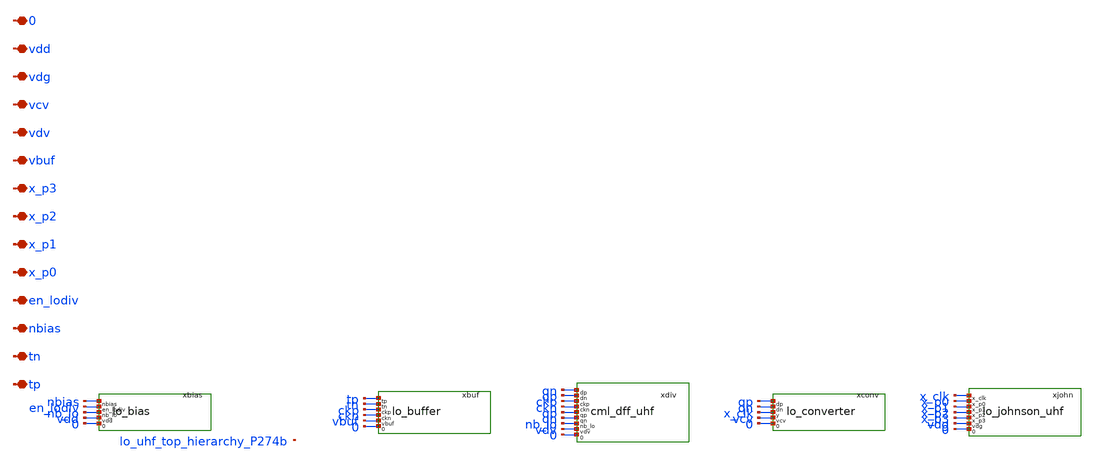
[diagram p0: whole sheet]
** sch_path: analog/lo/sch/lo_uhf_top.sch
**.subckt lo_uhf_top tp tn nbias en_lodiv x_p0 x_p1 x_p2 x_p3 vbuf vdv vcv vdg vdd 0
*.iopin tp
*.iopin tn
*.iopin nbias
*.iopin en_lodiv
*.iopin x_p0
*.iopin x_p1
*.iopin x_p2
*.iopin x_p3
*.iopin vbuf
*.iopin vdv
*.iopin vcv
*.iopin vdg
*.iopin vdd
*.iopin 0
xbias nbias en_lodiv nb_lo vdd 0 lo_bias
xbuf tp tn ckp ckn vbuf 0 lo_buffer
xdiv qn qp ckp ckn qp qn nb_lo vdv 0 cml_dff_uhf
xconv qp qn x_clk vcv 0 lo_converter
xjohn x_clk x_p0 x_p1 x_p2 x_p3 vdg 0 lo_johnson_uhf
**.ends

* expanding   symbol:  lo_bias.sym # of pins=5
** sym_path: analog/lo/sch/lo_bias.sym
** sch_path: analog/lo/sch/lo_bias.sch
.subckt lo_bias nbias en_lodiv nb_lo vdd 0
*.iopin nbias
*.iopin en_lodiv
*.iopin nb_lo
*.iopin vdd
*.iopin 0
Xxenb_p en_n en_lodiv vdd vdd sg13_lv_pmos w=1u l=0.13u ng=1 m=1 mm_ok=1
Xxenb_n en_n en_lodiv 0 0 sg13_lv_nmos w=0.5u l=0.13u ng=1 m=1 mm_ok=1
Xtgn nb_lo en_lodiv nbias 0 sg13_lv_nmos w=4u l=0.13u ng=1 m=1 mm_ok=1
Xtgp nb_lo en_n nbias vdd sg13_lv_pmos w=8u l=0.13u ng=1 m=1 mm_ok=1
Xmpd nb_lo en_n 0 0 sg13_lv_nmos w=2u l=0.13u ng=1 m=1 mm_ok=1
.ends


* expanding   symbol:  lo_buffer.sym # of pins=6
** sym_path: analog/lo/sch/lo_buffer.sym
** sch_path: analog/lo/sch/lo_buffer.sch
.subckt lo_buffer tp tn ckp ckn vbuf 0
*.iopin tp
*.iopin tn
*.iopin ckp
*.iopin ckn
*.iopin vbuf
*.iopin 0
ccp tp x_bip 100f m=1
rfp x_bip x_bop 50k m=1
Xxb1pp x_bop x_bip vbuf vbuf sg13_lv_pmos w=4u l=0.13u ng=1 m=1 mm_ok=1
Xxb1pn x_bop x_bip 0 0 sg13_lv_nmos w=2u l=0.13u ng=1 m=1 mm_ok=1
ccmp x_bop x_mip 50f m=1
rfmp x_mip x_bmp 50k m=1
Xxbmpp x_bmp x_mip vbuf vbuf sg13_lv_pmos w=6u l=0.13u ng=1 m=1 mm_ok=1
Xxbmpn x_bmp x_mip 0 0 sg13_lv_nmos w=3u l=0.13u ng=1 m=1 mm_ok=1
Xxb2pp ckp x_bmp vbuf vbuf sg13_lv_pmos w=8.0u l=0.13u ng=1 m=1 mm_ok=1
Xxb2pn ckp x_bmp 0 0 sg13_lv_nmos w=4.0u l=0.13u ng=1 m=1 mm_ok=1
ccn tn x_bin 100f m=1
rfn x_bin x_bon 50k m=1
Xxb1np x_bon x_bin vbuf vbuf sg13_lv_pmos w=4u l=0.13u ng=1 m=1 mm_ok=1
Xxb1nn x_bon x_bin 0 0 sg13_lv_nmos w=2u l=0.13u ng=1 m=1 mm_ok=1
ccmn x_bon x_min 50f m=1
rfmn x_min x_bmn 50k m=1
Xxbmnp x_bmn x_min vbuf vbuf sg13_lv_pmos w=6u l=0.13u ng=1 m=1 mm_ok=1
Xxbmnn x_bmn x_min 0 0 sg13_lv_nmos w=3u l=0.13u ng=1 m=1 mm_ok=1
Xxb2np ckn x_bmn vbuf vbuf sg13_lv_pmos w=8.0u l=0.13u ng=1 m=1 mm_ok=1
Xxb2nn ckn x_bmn 0 0 sg13_lv_nmos w=4.0u l=0.13u ng=1 m=1 mm_ok=1
Xxbxpp x_bon x_bop vbuf vbuf sg13_lv_pmos w=1u l=0.13u ng=1 m=1 mm_ok=1
Xxbxpn x_bon x_bop 0 0 sg13_lv_nmos w=0.5u l=0.13u ng=1 m=1 mm_ok=1
Xxbxnp x_bop x_bon vbuf vbuf sg13_lv_pmos w=1u l=0.13u ng=1 m=1 mm_ok=1
Xxbxnn x_bop x_bon 0 0 sg13_lv_nmos w=0.5u l=0.13u ng=1 m=1 mm_ok=1
Xxbopp ckn ckp vbuf vbuf sg13_lv_pmos w=2u l=0.13u ng=1 m=1 mm_ok=1
Xxbopn ckn ckp 0 0 sg13_lv_nmos w=1u l=0.13u ng=1 m=1 mm_ok=1
Xxbonp ckp ckn vbuf vbuf sg13_lv_pmos w=2u l=0.13u ng=1 m=1 mm_ok=1
Xxbonn ckp ckn 0 0 sg13_lv_nmos w=1u l=0.13u ng=1 m=1 mm_ok=1
.ends


* expanding   symbol:  cml_dff_uhf.sym # of pins=9
** sym_path: analog/lo/sch/cml_dff_uhf.sym
** sch_path: analog/lo/sch/cml_dff_uhf.sch
.subckt cml_dff_uhf dp dn ckp ckn qp qn nb_lo vdv 0
*.iopin dp
*.iopin dn
*.iopin ckp
*.iopin ckn
*.iopin qp
*.iopin qn
*.iopin nb_lo
*.iopin vdv
*.iopin 0
rlamp vdv map 666.7 m=1
rlamn vdv man 666.7 m=1
Xmam1 man dp s1am 0 sg13_lv_nmos w=7.50u l=0.13u ng=1 m=1 mm_ok=1
Xmam2 map dn s1am 0 sg13_lv_nmos w=7.50u l=0.13u ng=1 m=1 mm_ok=1
Xmam3 man map s2am 0 sg13_lv_nmos w=11.25u l=0.13u ng=1 m=1 mm_ok=1
Xmam4 map man s2am 0 sg13_lv_nmos w=11.25u l=0.13u ng=1 m=1 mm_ok=1
Xmam5 s1am ckp tam 0 sg13_lv_nmos w=7.50u l=0.13u ng=1 m=1 mm_ok=1
Xmam6 s2am ckn tam 0 sg13_lv_nmos w=7.50u l=0.13u ng=1 m=1 mm_ok=1
Xmtam tam nb_lo 0 0 sg13_lv_nmos w=15u l=0.13u ng=1 m=1 mm_ok=1
rlasp vdv qp 666.7 m=1
rlasn vdv qn 666.7 m=1
Xmas1 qn map s1as 0 sg13_lv_nmos w=7.50u l=0.13u ng=1 m=1 mm_ok=1
Xmas2 qp man s1as 0 sg13_lv_nmos w=7.50u l=0.13u ng=1 m=1 mm_ok=1
Xmas3 qn qp s2as 0 sg13_lv_nmos w=11.25u l=0.13u ng=1 m=1 mm_ok=1
Xmas4 qp qn s2as 0 sg13_lv_nmos w=11.25u l=0.13u ng=1 m=1 mm_ok=1
Xmas5 s1as ckn tas 0 sg13_lv_nmos w=7.50u l=0.13u ng=1 m=1 mm_ok=1
Xmas6 s2as ckp tas 0 sg13_lv_nmos w=7.50u l=0.13u ng=1 m=1 mm_ok=1
Xmtas tas nb_lo 0 0 sg13_lv_nmos w=15u l=0.13u ng=1 m=1 mm_ok=1
.ends


* expanding   symbol:  lo_converter.sym # of pins=5
** sym_path: analog/lo/sch/lo_converter.sym
** sch_path: analog/lo/sch/lo_converter.sch
.subckt lo_converter dp dn y vcv 0
*.iopin dp
*.iopin dn
*.iopin y
*.iopin vcv
*.iopin 0
ccap dp x_cip 50f m=1
rcap x_cip x_o2p 50k m=1
Xxcapp x_o2p x_cip vcv vcv sg13_lv_pmos w=4u l=0.13u ng=1 m=1 mm_ok=1
Xxcapn x_o2p x_cip 0 0 sg13_lv_nmos w=2u l=0.13u ng=1 m=1 mm_ok=1
ccan dn x_cin 50f m=1
rcan x_cin x_o2n 50k m=1
Xxcanp x_o2n x_cin vcv vcv sg13_lv_pmos w=4u l=0.13u ng=1 m=1 mm_ok=1
Xxcann x_o2n x_cin 0 0 sg13_lv_nmos w=2u l=0.13u ng=1 m=1 mm_ok=1
Xxcxpp x_o2n x_o2p vcv vcv sg13_lv_pmos w=1u l=0.13u ng=1 m=1 mm_ok=1
Xxcxpn x_o2n x_o2p 0 0 sg13_lv_nmos w=0.5u l=0.13u ng=1 m=1 mm_ok=1
Xxcxnp x_o2p x_o2n vcv vcv sg13_lv_pmos w=1u l=0.13u ng=1 m=1 mm_ok=1
Xxcxnn x_o2p x_o2n 0 0 sg13_lv_nmos w=0.5u l=0.13u ng=1 m=1 mm_ok=1
ccb x_o2p x_cbi 50f m=1
rcb x_cbi x_cy 50k m=1
Xxcbp x_cy x_cbi vcv vcv sg13_lv_pmos w=4u l=0.13u ng=1 m=1 mm_ok=1
Xxcbn x_cy x_cbi 0 0 sg13_lv_nmos w=2u l=0.13u ng=1 m=1 mm_ok=1
Xxcv3p x_cz x_cy vcv vcv sg13_lv_pmos w=6.0u l=0.13u ng=1 m=1 mm_ok=1
Xxcv3n x_cz x_cy 0 0 sg13_lv_nmos w=3.0u l=0.13u ng=1 m=1 mm_ok=1
Xxcv4p y x_cz vcv vcv sg13_lv_pmos w=18.0u l=0.13u ng=1 m=1 mm_ok=1
Xxcv4n y x_cz 0 0 sg13_lv_nmos w=9.0u l=0.13u ng=1 m=1 mm_ok=1
.ends


* expanding   symbol:  lo_johnson_uhf.sym # of pins=7
** sym_path: analog/lo/sch/lo_johnson_uhf.sym
** sch_path: analog/lo/sch/lo_johnson_uhf.sch
.subckt lo_johnson_uhf x_clk x_p0 x_p1 x_p2 x_p3 vdg 0
*.iopin x_clk
*.iopin x_p0
*.iopin x_p1
*.iopin x_p2
*.iopin x_p3
*.iopin vdg
*.iopin 0
Xxf1p1 x_f1_x1 x_q2 vdg vdg sg13_lv_pmos w=2u l=0.13u ng=1 m=1 mm_ok=1
Xxf1p2 x_f1_a x_clk x_f1_x1 vdg sg13_lv_pmos w=2u l=0.13u ng=1 m=1 mm_ok=1
Xxf1n1 x_f1_a x_q2 0 0 sg13_lv_nmos w=1u l=0.13u ng=1 m=1 mm_ok=1
Xxf1p3 x_f1_b x_clk vdg vdg sg13_lv_pmos w=2u l=0.13u ng=1 m=1 mm_ok=1
Xxf1n2 x_f1_b x_f1_a x_f1_x2 0 sg13_lv_nmos w=1u l=0.13u ng=1 m=1 mm_ok=1
Xxf1n3 x_f1_x2 x_clk 0 0 sg13_lv_nmos w=1u l=0.13u ng=1 m=1 mm_ok=1
Xxf1p4 x_q1 x_f1_b vdg vdg sg13_lv_pmos w=2u l=0.13u ng=1 m=1 mm_ok=1
Xxf1n4 x_q1 x_clk x_f1_x3 0 sg13_lv_nmos w=1u l=0.13u ng=1 m=1 mm_ok=1
Xxf1n5 x_f1_x3 x_f1_b 0 0 sg13_lv_nmos w=1u l=0.13u ng=1 m=1 mm_ok=1
Xxi1p x_q1b x_q1 vdg vdg sg13_lv_pmos w=1.0u l=0.13u ng=1 m=1 mm_ok=1
Xxi1n x_q1b x_q1 0 0 sg13_lv_nmos w=0.5u l=0.13u ng=1 m=1 mm_ok=1
Xxf2p1 x_f2_x1 x_q1b vdg vdg sg13_lv_pmos w=2u l=0.13u ng=1 m=1 mm_ok=1
Xxf2p2 x_f2_a x_clk x_f2_x1 vdg sg13_lv_pmos w=2u l=0.13u ng=1 m=1 mm_ok=1
Xxf2n1 x_f2_a x_q1b 0 0 sg13_lv_nmos w=1u l=0.13u ng=1 m=1 mm_ok=1
Xxf2p3 x_f2_b x_clk vdg vdg sg13_lv_pmos w=2u l=0.13u ng=1 m=1 mm_ok=1
Xxf2n2 x_f2_b x_f2_a x_f2_x2 0 sg13_lv_nmos w=1u l=0.13u ng=1 m=1 mm_ok=1
Xxf2n3 x_f2_x2 x_clk 0 0 sg13_lv_nmos w=1u l=0.13u ng=1 m=1 mm_ok=1
Xxf2p4 x_q2 x_f2_b vdg vdg sg13_lv_pmos w=2u l=0.13u ng=1 m=1 mm_ok=1
Xxf2n4 x_q2 x_clk x_f2_x3 0 sg13_lv_nmos w=1u l=0.13u ng=1 m=1 mm_ok=1
Xxf2n5 x_f2_x3 x_f2_b 0 0 sg13_lv_nmos w=1u l=0.13u ng=1 m=1 mm_ok=1
Xxi2p x_q2b x_q2 vdg vdg sg13_lv_pmos w=1.0u l=0.13u ng=1 m=1 mm_ok=1
Xxi2n x_q2b x_q2 0 0 sg13_lv_nmos w=0.5u l=0.13u ng=1 m=1 mm_ok=1
Xxg0pa x_n0 x_q1 vdg vdg sg13_lv_pmos w=1u l=0.13u ng=1 m=1 mm_ok=1
Xxg0pb x_n0 x_q2b vdg vdg sg13_lv_pmos w=1u l=0.13u ng=1 m=1 mm_ok=1
Xxg0na x_n0 x_q1 x_g0m 0 sg13_lv_nmos w=1u l=0.13u ng=1 m=1 mm_ok=1
Xxg0nb x_g0m x_q2b 0 0 sg13_lv_nmos w=1u l=0.13u ng=1 m=1 mm_ok=1
Xxr0p1 x_r0_x1 x_n0 vdg vdg sg13_lv_pmos w=2u l=0.13u ng=1 m=1 mm_ok=1
Xxr0p2 x_r0_a x_clk x_r0_x1 vdg sg13_lv_pmos w=2u l=0.13u ng=1 m=1 mm_ok=1
Xxr0n1 x_r0_a x_n0 0 0 sg13_lv_nmos w=1u l=0.13u ng=1 m=1 mm_ok=1
Xxr0p3 x_r0_b x_clk vdg vdg sg13_lv_pmos w=2u l=0.13u ng=1 m=1 mm_ok=1
Xxr0n2 x_r0_b x_r0_a x_r0_x2 0 sg13_lv_nmos w=1u l=0.13u ng=1 m=1 mm_ok=1
Xxr0n3 x_r0_x2 x_clk 0 0 sg13_lv_nmos w=1u l=0.13u ng=1 m=1 mm_ok=1
Xxr0p4 x_p0 x_r0_b vdg vdg sg13_lv_pmos w=4u l=0.13u ng=1 m=1 mm_ok=1
Xxr0n4 x_p0 x_clk x_r0_x3 0 sg13_lv_nmos w=1u l=0.13u ng=1 m=1 mm_ok=1
Xxr0n5 x_r0_x3 x_r0_b 0 0 sg13_lv_nmos w=1u l=0.13u ng=1 m=1 mm_ok=1
cpl0 x_p0 0 20f m=1
Xxg1pa x_n1 x_q1 vdg vdg sg13_lv_pmos w=1u l=0.13u ng=1 m=1 mm_ok=1
Xxg1pb x_n1 x_q2 vdg vdg sg13_lv_pmos w=1u l=0.13u ng=1 m=1 mm_ok=1
Xxg1na x_n1 x_q1 x_g1m 0 sg13_lv_nmos w=1u l=0.13u ng=1 m=1 mm_ok=1
Xxg1nb x_g1m x_q2 0 0 sg13_lv_nmos w=1u l=0.13u ng=1 m=1 mm_ok=1
Xxr1p1 x_r1_x1 x_n1 vdg vdg sg13_lv_pmos w=2u l=0.13u ng=1 m=1 mm_ok=1
Xxr1p2 x_r1_a x_clk x_r1_x1 vdg sg13_lv_pmos w=2u l=0.13u ng=1 m=1 mm_ok=1
Xxr1n1 x_r1_a x_n1 0 0 sg13_lv_nmos w=1u l=0.13u ng=1 m=1 mm_ok=1
Xxr1p3 x_r1_b x_clk vdg vdg sg13_lv_pmos w=2u l=0.13u ng=1 m=1 mm_ok=1
Xxr1n2 x_r1_b x_r1_a x_r1_x2 0 sg13_lv_nmos w=1u l=0.13u ng=1 m=1 mm_ok=1
Xxr1n3 x_r1_x2 x_clk 0 0 sg13_lv_nmos w=1u l=0.13u ng=1 m=1 mm_ok=1
Xxr1p4 x_p1 x_r1_b vdg vdg sg13_lv_pmos w=4u l=0.13u ng=1 m=1 mm_ok=1
Xxr1n4 x_p1 x_clk x_r1_x3 0 sg13_lv_nmos w=1u l=0.13u ng=1 m=1 mm_ok=1
Xxr1n5 x_r1_x3 x_r1_b 0 0 sg13_lv_nmos w=1u l=0.13u ng=1 m=1 mm_ok=1
cpl1 x_p1 0 20f m=1
Xxg2pa x_n2 x_q1b vdg vdg sg13_lv_pmos w=1u l=0.13u ng=1 m=1 mm_ok=1
Xxg2pb x_n2 x_q2 vdg vdg sg13_lv_pmos w=1u l=0.13u ng=1 m=1 mm_ok=1
Xxg2na x_n2 x_q1b x_g2m 0 sg13_lv_nmos w=1u l=0.13u ng=1 m=1 mm_ok=1
Xxg2nb x_g2m x_q2 0 0 sg13_lv_nmos w=1u l=0.13u ng=1 m=1 mm_ok=1
Xxr2p1 x_r2_x1 x_n2 vdg vdg sg13_lv_pmos w=2u l=0.13u ng=1 m=1 mm_ok=1
Xxr2p2 x_r2_a x_clk x_r2_x1 vdg sg13_lv_pmos w=2u l=0.13u ng=1 m=1 mm_ok=1
Xxr2n1 x_r2_a x_n2 0 0 sg13_lv_nmos w=1u l=0.13u ng=1 m=1 mm_ok=1
Xxr2p3 x_r2_b x_clk vdg vdg sg13_lv_pmos w=2u l=0.13u ng=1 m=1 mm_ok=1
Xxr2n2 x_r2_b x_r2_a x_r2_x2 0 sg13_lv_nmos w=1u l=0.13u ng=1 m=1 mm_ok=1
Xxr2n3 x_r2_x2 x_clk 0 0 sg13_lv_nmos w=1u l=0.13u ng=1 m=1 mm_ok=1
Xxr2p4 x_p2 x_r2_b vdg vdg sg13_lv_pmos w=4u l=0.13u ng=1 m=1 mm_ok=1
Xxr2n4 x_p2 x_clk x_r2_x3 0 sg13_lv_nmos w=1u l=0.13u ng=1 m=1 mm_ok=1
Xxr2n5 x_r2_x3 x_r2_b 0 0 sg13_lv_nmos w=1u l=0.13u ng=1 m=1 mm_ok=1
cpl2 x_p2 0 20f m=1
Xxg3pa x_n3 x_q1b vdg vdg sg13_lv_pmos w=1u l=0.13u ng=1 m=1 mm_ok=1
Xxg3pb x_n3 x_q2b vdg vdg sg13_lv_pmos w=1u l=0.13u ng=1 m=1 mm_ok=1
Xxg3na x_n3 x_q1b x_g3m 0 sg13_lv_nmos w=1u l=0.13u ng=1 m=1 mm_ok=1
Xxg3nb x_g3m x_q2b 0 0 sg13_lv_nmos w=1u l=0.13u ng=1 m=1 mm_ok=1
Xxr3p1 x_r3_x1 x_n3 vdg vdg sg13_lv_pmos w=2u l=0.13u ng=1 m=1 mm_ok=1
Xxr3p2 x_r3_a x_clk x_r3_x1 vdg sg13_lv_pmos w=2u l=0.13u ng=1 m=1 mm_ok=1
Xxr3n1 x_r3_a x_n3 0 0 sg13_lv_nmos w=1u l=0.13u ng=1 m=1 mm_ok=1
Xxr3p3 x_r3_b x_clk vdg vdg sg13_lv_pmos w=2u l=0.13u ng=1 m=1 mm_ok=1
Xxr3n2 x_r3_b x_r3_a x_r3_x2 0 sg13_lv_nmos w=1u l=0.13u ng=1 m=1 mm_ok=1
Xxr3n3 x_r3_x2 x_clk 0 0 sg13_lv_nmos w=1u l=0.13u ng=1 m=1 mm_ok=1
Xxr3p4 x_p3 x_r3_b vdg vdg sg13_lv_pmos w=4u l=0.13u ng=1 m=1 mm_ok=1
Xxr3n4 x_p3 x_clk x_r3_x3 0 sg13_lv_nmos w=1u l=0.13u ng=1 m=1 mm_ok=1
Xxr3n5 x_r3_x3 x_r3_b 0 0 sg13_lv_nmos w=1u l=0.13u ng=1 m=1 mm_ok=1
cpl3 x_p3 0 20f m=1
Xxf1kq1p x_f1_kq x_q1 vdg vdg sg13_lv_pmos w=0.3u l=0.13u ng=1 m=1 mm_ok=1
Xxf1kq1n x_f1_kq x_q1 0 0 sg13_lv_nmos w=0.15u l=0.13u ng=1 m=1 mm_ok=1
Xxf1kq2p x_q1 x_f1_kq vdg vdg sg13_lv_pmos w=0.3u l=0.13u ng=1 m=1 mm_ok=1
Xxf1kq2n x_q1 x_f1_kq 0 0 sg13_lv_nmos w=0.15u l=0.13u ng=1 m=1 mm_ok=1
rkf11 x_f1_a 0 100Meg m=1
rkf12 x_f1_b 0 100Meg m=1
Xxf2kq1p x_f2_kq x_q2 vdg vdg sg13_lv_pmos w=0.3u l=0.13u ng=1 m=1 mm_ok=1
Xxf2kq1n x_f2_kq x_q2 0 0 sg13_lv_nmos w=0.15u l=0.13u ng=1 m=1 mm_ok=1
Xxf2kq2p x_q2 x_f2_kq vdg vdg sg13_lv_pmos w=0.3u l=0.13u ng=1 m=1 mm_ok=1
Xxf2kq2n x_q2 x_f2_kq 0 0 sg13_lv_nmos w=0.15u l=0.13u ng=1 m=1 mm_ok=1
rkf21 x_f2_a 0 100Meg m=1
rkf22 x_f2_b 0 100Meg m=1
Xxr0kq1p x_r0_kq x_p0 vdg vdg sg13_lv_pmos w=0.3u l=0.13u ng=1 m=1 mm_ok=1
Xxr0kq1n x_r0_kq x_p0 0 0 sg13_lv_nmos w=0.15u l=0.13u ng=1 m=1 mm_ok=1
Xxr0kq2p x_p0 x_r0_kq vdg vdg sg13_lv_pmos w=0.3u l=0.13u ng=1 m=1 mm_ok=1
Xxr0kq2n x_p0 x_r0_kq 0 0 sg13_lv_nmos w=0.15u l=0.13u ng=1 m=1 mm_ok=1
rkr01 x_r0_a 0 100Meg m=1
rkr02 x_r0_b 0 100Meg m=1
Xxr1kq1p x_r1_kq x_p1 vdg vdg sg13_lv_pmos w=0.3u l=0.13u ng=1 m=1 mm_ok=1
Xxr1kq1n x_r1_kq x_p1 0 0 sg13_lv_nmos w=0.15u l=0.13u ng=1 m=1 mm_ok=1
Xxr1kq2p x_p1 x_r1_kq vdg vdg sg13_lv_pmos w=0.3u l=0.13u ng=1 m=1 mm_ok=1
Xxr1kq2n x_p1 x_r1_kq 0 0 sg13_lv_nmos w=0.15u l=0.13u ng=1 m=1 mm_ok=1
rkr11 x_r1_a 0 100Meg m=1
rkr12 x_r1_b 0 100Meg m=1
Xxr2kq1p x_r2_kq x_p2 vdg vdg sg13_lv_pmos w=0.3u l=0.13u ng=1 m=1 mm_ok=1
Xxr2kq1n x_r2_kq x_p2 0 0 sg13_lv_nmos w=0.15u l=0.13u ng=1 m=1 mm_ok=1
Xxr2kq2p x_p2 x_r2_kq vdg vdg sg13_lv_pmos w=0.3u l=0.13u ng=1 m=1 mm_ok=1
Xxr2kq2n x_p2 x_r2_kq 0 0 sg13_lv_nmos w=0.15u l=0.13u ng=1 m=1 mm_ok=1
rkr21 x_r2_a 0 100Meg m=1
rkr22 x_r2_b 0 100Meg m=1
Xxr3kq1p x_r3_kq x_p3 vdg vdg sg13_lv_pmos w=0.3u l=0.13u ng=1 m=1 mm_ok=1
Xxr3kq1n x_r3_kq x_p3 0 0 sg13_lv_nmos w=0.15u l=0.13u ng=1 m=1 mm_ok=1
Xxr3kq2p x_p3 x_r3_kq vdg vdg sg13_lv_pmos w=0.3u l=0.13u ng=1 m=1 mm_ok=1
Xxr3kq2n x_p3 x_r3_kq 0 0 sg13_lv_nmos w=0.15u l=0.13u ng=1 m=1 mm_ok=1
rkr31 x_r3_a 0 100Meg m=1
rkr32 x_r3_b 0 100Meg m=1
.ends

.end
